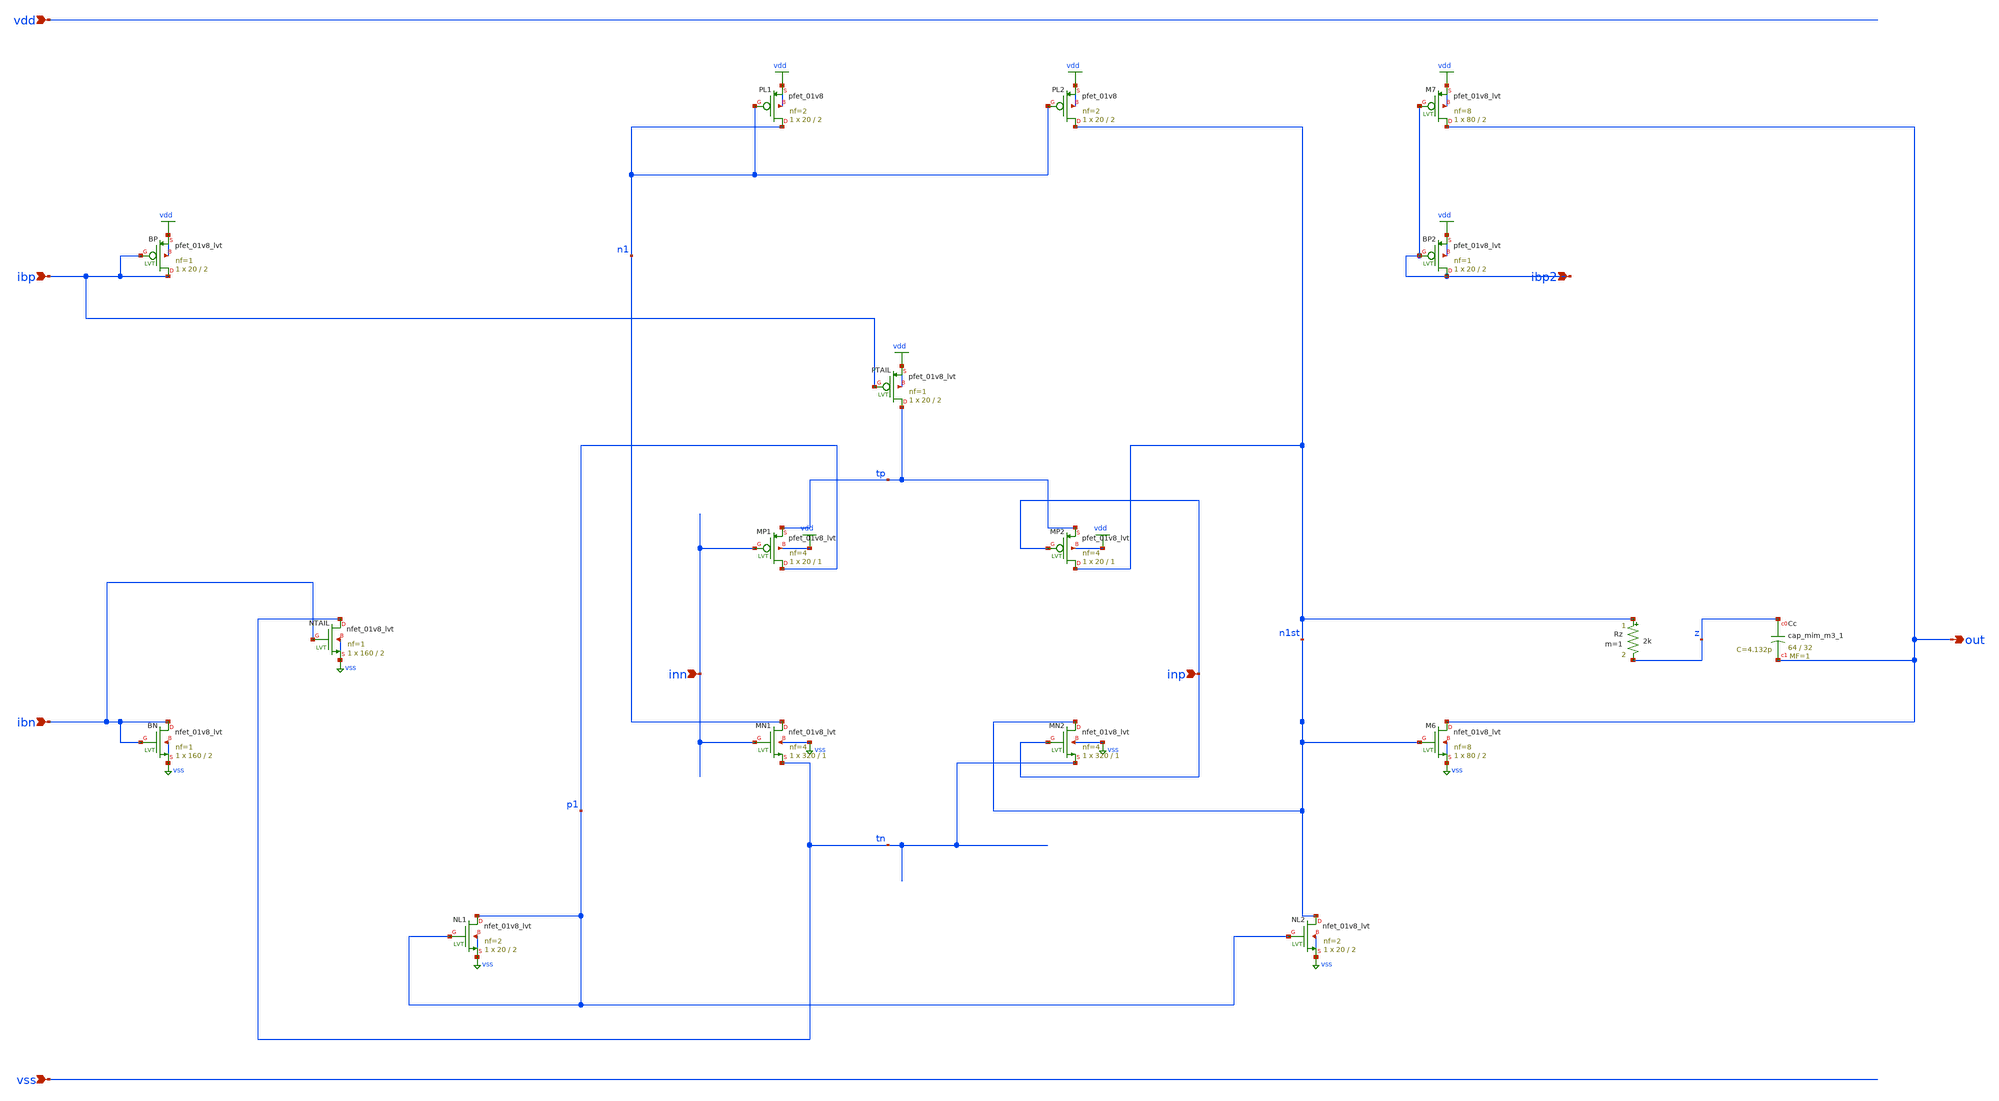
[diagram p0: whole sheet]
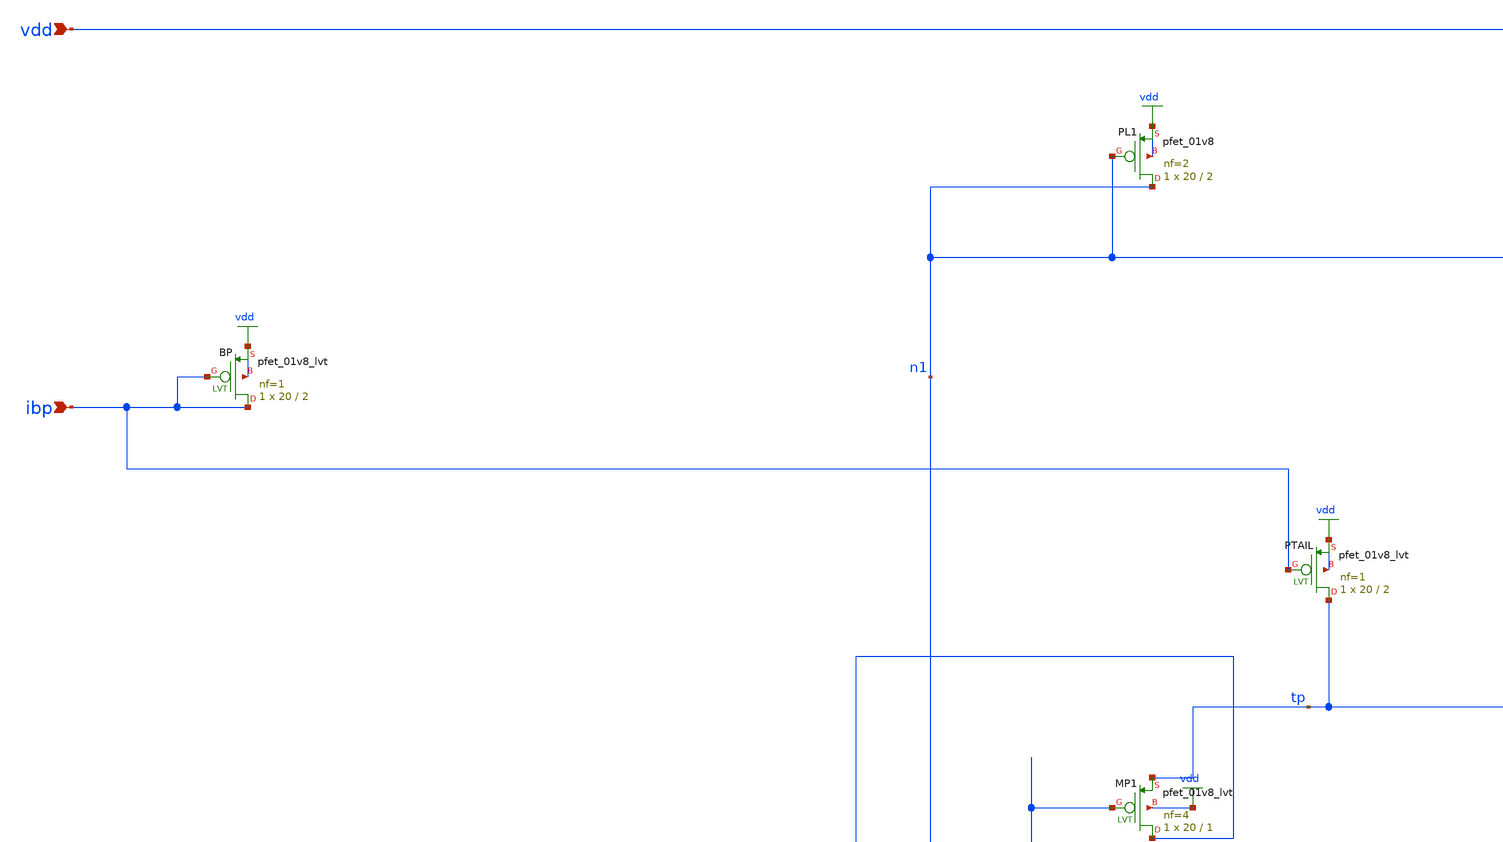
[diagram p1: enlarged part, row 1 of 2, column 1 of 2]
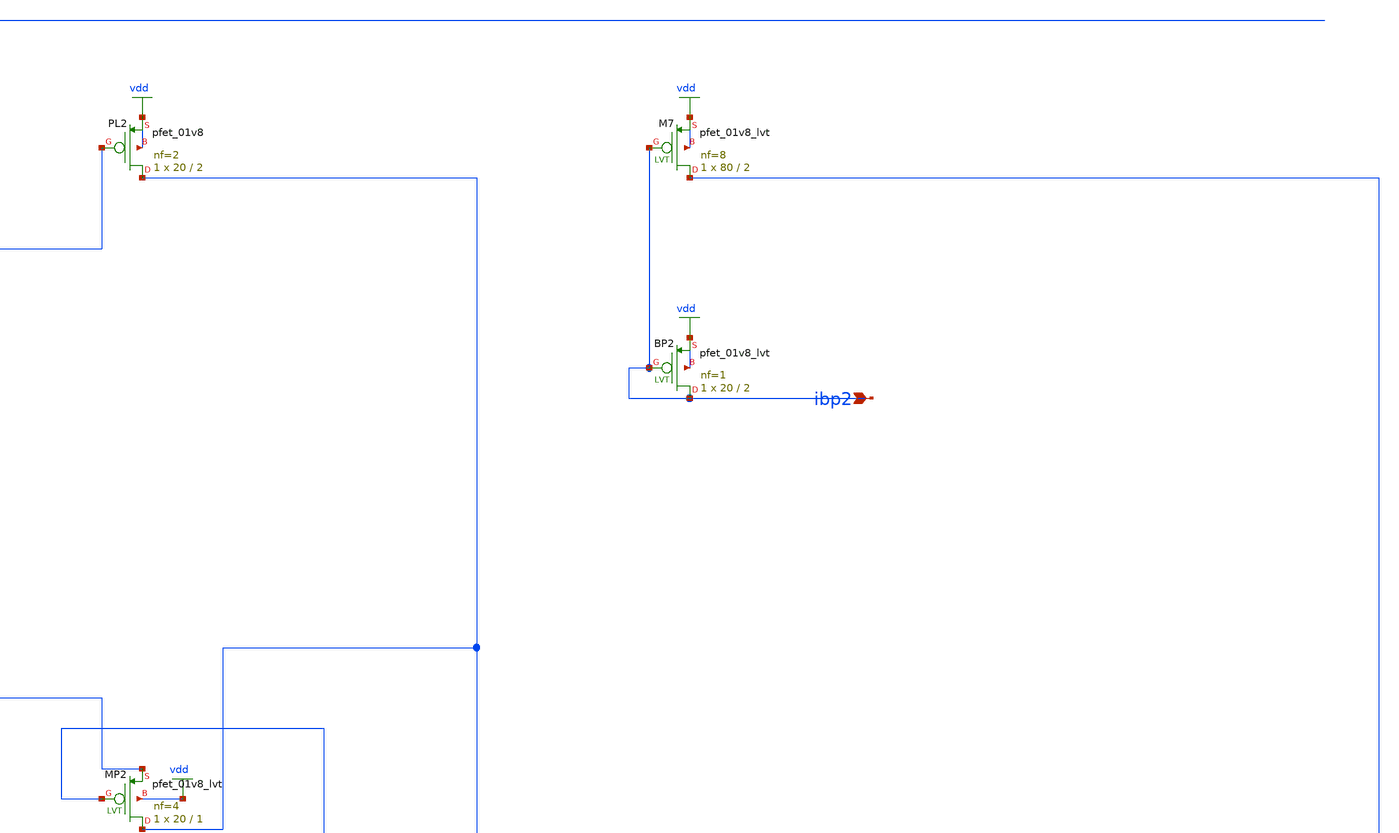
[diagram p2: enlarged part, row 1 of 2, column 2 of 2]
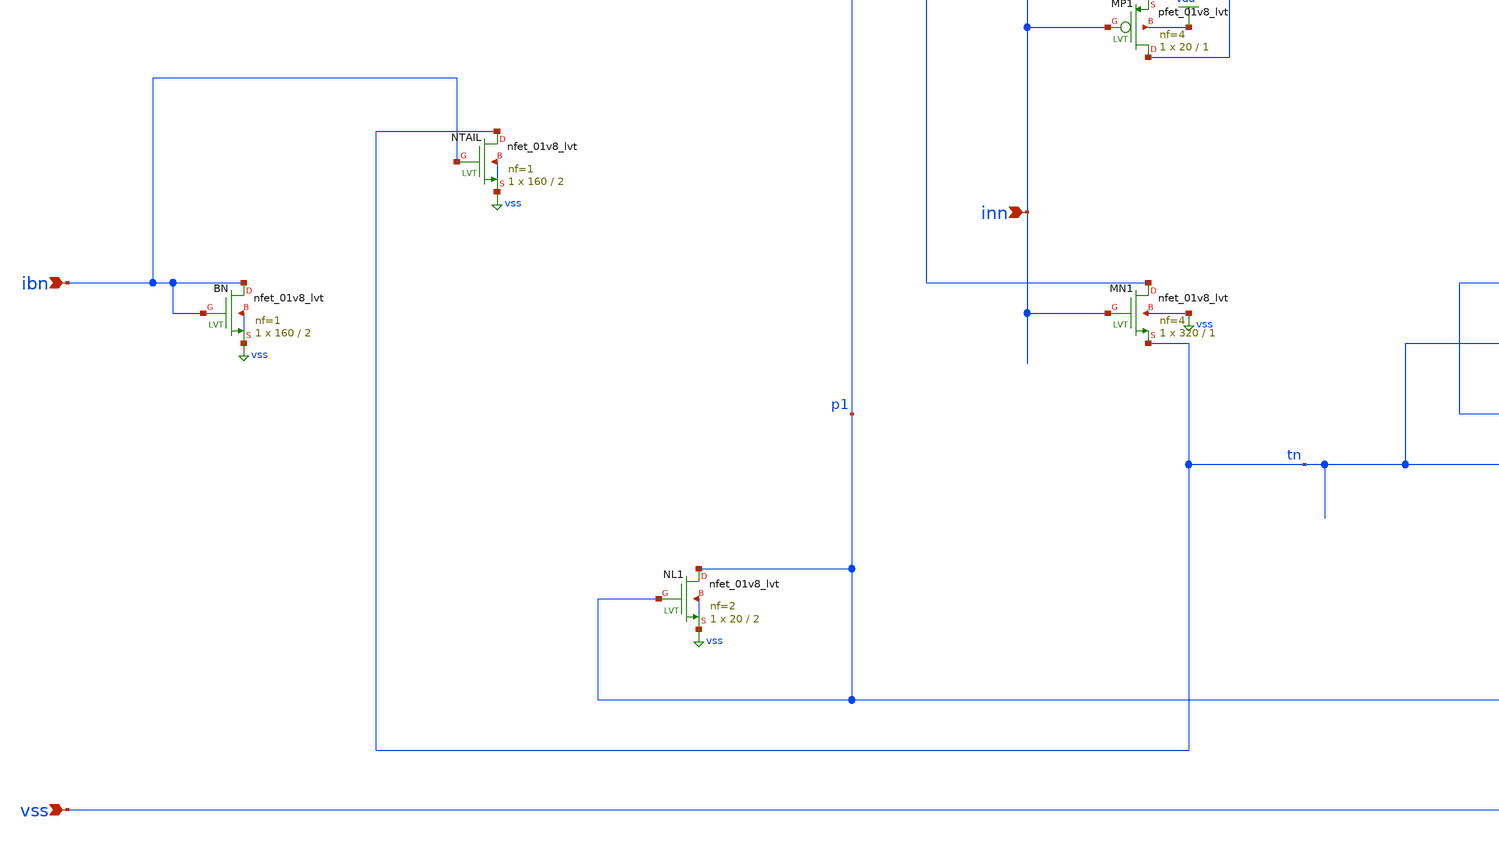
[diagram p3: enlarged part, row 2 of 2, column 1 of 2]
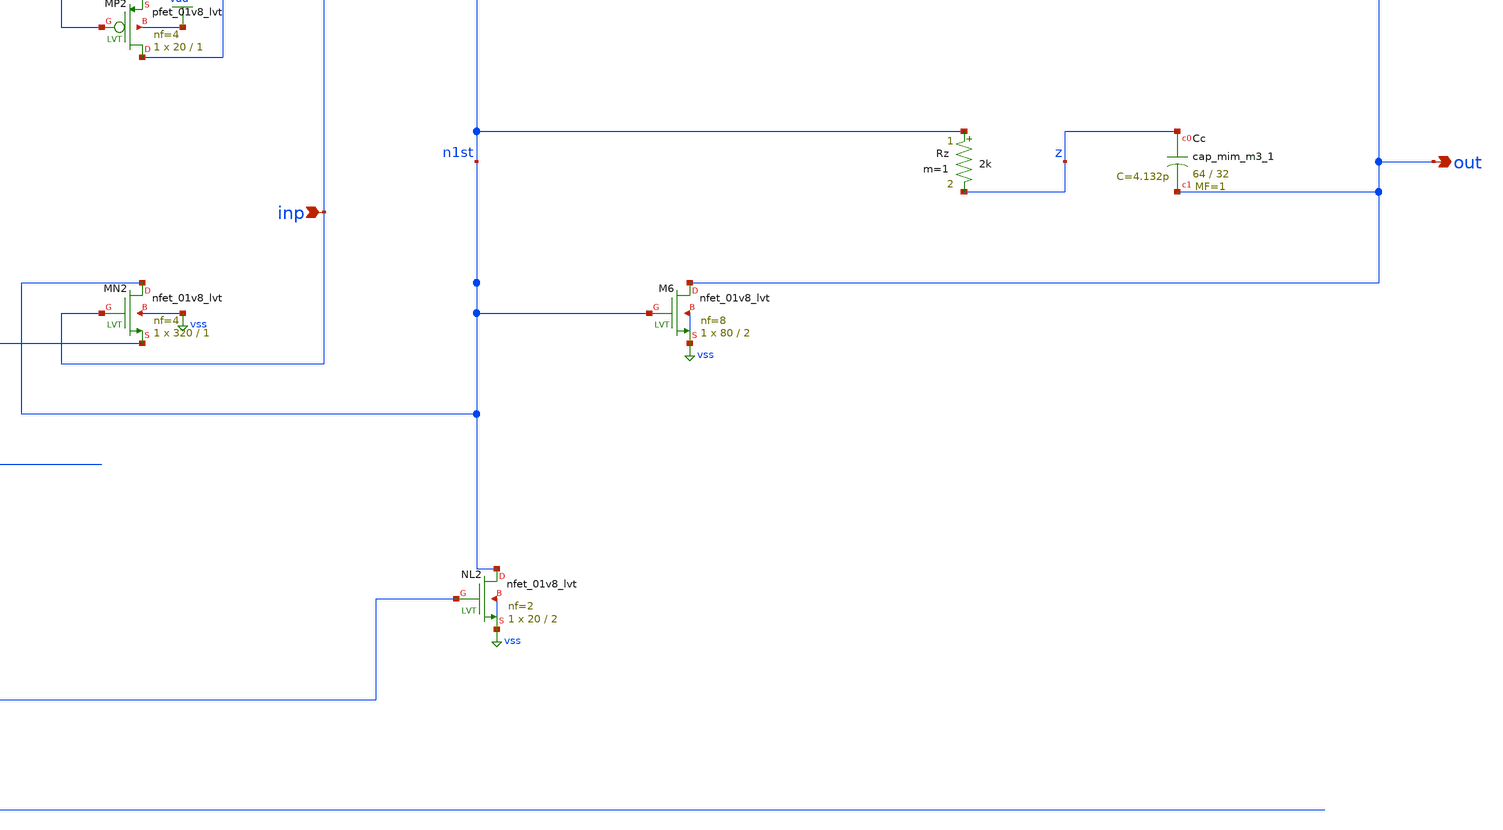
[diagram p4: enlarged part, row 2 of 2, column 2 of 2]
** sch_path: 10-sky130-analog-ic-design/schematics/opamp_rri_clean.sch
**.subckt opamp_rri_clean inp inn out vdd vss ibn ibp ibp2
*.ipin inp
*.ipin inn
*.opin out
*.ipin vdd
*.ipin vss
*.ipin ibn
*.ipin ibp
*.ipin ibp2
XBN ibn ibn vss vss sky130_fd_pr__nfet_01v8_lvt L=2 W=160 nf=1 ad='int((1 + 1)/2) * 160 / 1 * 0.29' as='int((1 + 2)/2) * 160 / 1 * 0.29'
+ pd='2*int((1 + 1)/2) * (160 / 1 + 0.29)' ps='2*int((1 + 2)/2) * (160 / 1 + 0.29)' nrd='0.29 / 160 ' nrs='0.29 / 160 '
+ sa=0 sb=0 sd=0 mult=1 m=1
XNTAIL tn ibn vss vss sky130_fd_pr__nfet_01v8_lvt L=2 W=160 nf=1 ad='int((1 + 1)/2) * 160 / 1 * 0.29'
+ as='int((1 + 2)/2) * 160 / 1 * 0.29' pd='2*int((1 + 1)/2) * (160 / 1 + 0.29)' ps='2*int((1 + 2)/2) * (160 / 1 + 0.29)'
+ nrd='0.29 / 160 ' nrs='0.29 / 160 ' sa=0 sb=0 sd=0 mult=1 m=1
XBP ibp ibp vdd vdd sky130_fd_pr__pfet_01v8_lvt L=2 W=20 nf=1 ad='int((1 + 1)/2) * 20 / 1 * 0.29' as='int((1 + 2)/2) * 20 / 1 * 0.29'
+ pd='2*int((1 + 1)/2) * (20 / 1 + 0.29)' ps='2*int((1 + 2)/2) * (20 / 1 + 0.29)' nrd='0.29 / 20 ' nrs='0.29 / 20 '
+ sa=0 sb=0 sd=0 mult=1 m=1
XPTAIL tp ibp vdd vdd sky130_fd_pr__pfet_01v8_lvt L=2 W=20 nf=1 ad='int((1 + 1)/2) * 20 / 1 * 0.29' as='int((1 + 2)/2) * 20 / 1 * 0.29'
+ pd='2*int((1 + 1)/2) * (20 / 1 + 0.29)' ps='2*int((1 + 2)/2) * (20 / 1 + 0.29)' nrd='0.29 / 20 ' nrs='0.29 / 20 '
+ sa=0 sb=0 sd=0 mult=1 m=1
XBP2 ibp2 ibp2 vdd vdd sky130_fd_pr__pfet_01v8_lvt L=2 W=20 nf=1 ad='int((1 + 1)/2) * 20 / 1 * 0.29'
+ as='int((1 + 2)/2) * 20 / 1 * 0.29' pd='2*int((1 + 1)/2) * (20 / 1 + 0.29)' ps='2*int((1 + 2)/2) * (20 / 1 + 0.29)'
+ nrd='0.29 / 20 ' nrs='0.29 / 20 ' sa=0 sb=0 sd=0 mult=1 m=1
XMN1 n1 inn tn vss sky130_fd_pr__nfet_01v8_lvt L=1 W=320 nf=4 ad='int((4 + 1)/2) * 320 / 4 * 0.29' as='int((4 + 2)/2) * 320 / 4 * 0.29'
+ pd='2*int((4 + 1)/2) * (320 / 4 + 0.29)' ps='2*int((4 + 2)/2) * (320 / 4 + 0.29)' nrd='0.29 / 320 ' nrs='0.29 / 320 '
+ sa=0 sb=0 sd=0 mult=1 m=1
XMN2 n1st inp tn vss sky130_fd_pr__nfet_01v8_lvt L=1 W=320 nf=4 ad='int((4 + 1)/2) * 320 / 4 * 0.29'
+ as='int((4 + 2)/2) * 320 / 4 * 0.29' pd='2*int((4 + 1)/2) * (320 / 4 + 0.29)' ps='2*int((4 + 2)/2) * (320 / 4 + 0.29)'
+ nrd='0.29 / 320 ' nrs='0.29 / 320 ' sa=0 sb=0 sd=0 mult=1 m=1
XMP1 p1 inn tp vdd sky130_fd_pr__pfet_01v8_lvt L=1 W=20 nf=4 ad='int((4 + 1)/2) * 20 / 4 * 0.29' as='int((4 + 2)/2) * 20 / 4 * 0.29'
+ pd='2*int((4 + 1)/2) * (20 / 4 + 0.29)' ps='2*int((4 + 2)/2) * (20 / 4 + 0.29)' nrd='0.29 / 20 ' nrs='0.29 / 20 '
+ sa=0 sb=0 sd=0 mult=1 m=1
XMP2 n1st inp tp vdd sky130_fd_pr__pfet_01v8_lvt L=1 W=20 nf=4 ad='int((4 + 1)/2) * 20 / 4 * 0.29' as='int((4 + 2)/2) * 20 / 4 * 0.29'
+ pd='2*int((4 + 1)/2) * (20 / 4 + 0.29)' ps='2*int((4 + 2)/2) * (20 / 4 + 0.29)' nrd='0.29 / 20 ' nrs='0.29 / 20 '
+ sa=0 sb=0 sd=0 mult=1 m=1
XPL1 n1 n1 vdd vdd sky130_fd_pr__pfet_01v8 L=2 W=20 nf=2 ad='int((nf+1)/2) * W/nf * 0.29' as='int((nf+2)/2) * W/nf * 0.29'
+ pd='2*int((nf+1)/2) * (W/nf + 0.29)' ps='2*int((nf+2)/2) * (W/nf + 0.29)' nrd='0.29 / W' nrs='0.29 / W'
+ sa=0 sb=0 sd=0 mult=1 m=1
XPL2 n1st n1 vdd vdd sky130_fd_pr__pfet_01v8 L=2 W=20 nf=2 ad='int((nf+1)/2) * W/nf * 0.29' as='int((nf+2)/2) * W/nf * 0.29'
+ pd='2*int((nf+1)/2) * (W/nf + 0.29)' ps='2*int((nf+2)/2) * (W/nf + 0.29)' nrd='0.29 / W' nrs='0.29 / W'
+ sa=0 sb=0 sd=0 mult=1 m=1
XNL1 p1 p1 vss vss sky130_fd_pr__nfet_01v8_lvt L=2 W=20 nf=2 ad='int((2 + 1)/2) * 20 / 2 * 0.29' as='int((2 + 2)/2) * 20 / 2 * 0.29'
+ pd='2*int((2 + 1)/2) * (20 / 2 + 0.29)' ps='2*int((2 + 2)/2) * (20 / 2 + 0.29)' nrd='0.29 / 20 ' nrs='0.29 / 20 '
+ sa=0 sb=0 sd=0 mult=1 m=1
XNL2 n1st p1 vss vss sky130_fd_pr__nfet_01v8_lvt L=2 W=20 nf=2 ad='int((2 + 1)/2) * 20 / 2 * 0.29' as='int((2 + 2)/2) * 20 / 2 * 0.29'
+ pd='2*int((2 + 1)/2) * (20 / 2 + 0.29)' ps='2*int((2 + 2)/2) * (20 / 2 + 0.29)' nrd='0.29 / 20 ' nrs='0.29 / 20 '
+ sa=0 sb=0 sd=0 mult=1 m=1
XM6 out n1st vss vss sky130_fd_pr__nfet_01v8_lvt L=2 W=80 nf=8 ad='int((8 + 1)/2) * 80 / 8 * 0.29' as='int((8 + 2)/2) * 80 / 8 * 0.29'
+ pd='2*int((8 + 1)/2) * (80 / 8 + 0.29)' ps='2*int((8 + 2)/2) * (80 / 8 + 0.29)' nrd='0.29 / 80 ' nrs='0.29 / 80 '
+ sa=0 sb=0 sd=0 mult=1 m=1
XM7 out ibp2 vdd vdd sky130_fd_pr__pfet_01v8_lvt L=2 W=80 nf=8 ad='int((8 + 1)/2) * 80 / 8 * 0.29' as='int((8 + 2)/2) * 80 / 8 * 0.29'
+ pd='2*int((8 + 1)/2) * (80 / 8 + 0.29)' ps='2*int((8 + 2)/2) * (80 / 8 + 0.29)' nrd='0.29 / 80 ' nrs='0.29 / 80 '
+ sa=0 sb=0 sd=0 mult=1 m=1
Rz n1st z 2k m=1
XCc z out sky130_fd_pr__cap_mim_m3_1 W=64 L=32 MF=1 m=1
**.ends
.GLOBAL vdd
.GLOBAL vss
.end
